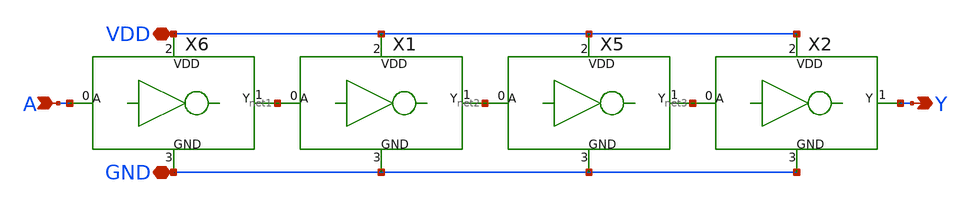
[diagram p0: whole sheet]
** sch_path: Tutorials/1-3_Inverter_Netgen/buffer.sch
**.subckt buffer A Y VDD GND
*.ipin A
*.opin Y
*.iopin VDD
*.iopin GND
X6 A net1 VDD GND inverter
X1 net1 net2 VDD GND inverter
X5 net2 net3 VDD GND inverter
X2 net3 Y VDD GND inverter
**.ends
.end
